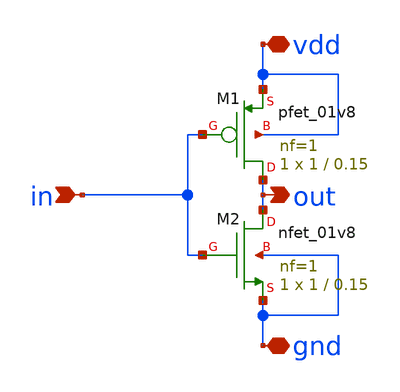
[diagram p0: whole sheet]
** sch_path: inverter.sch
**.subckt inverter in vdd gnd out
*.ipin in
*.iopin vdd
*.iopin gnd
*.opin out
XM1 out in vdd vdd sky130_fd_pr__pfet_01v8 L=0.15 W=1 nf=1 ad='int((1 + 1)/2) * 1 / 1 * 0.29' as='int((1 + 2)/2) * 1 / 1 * 0.29'
+ pd='2*int((1 + 1)/2) * (1 / 1 + 0.29)' ps='2*int((1 + 2)/2) * (1 / 1 + 0.29)' nrd='0.29 / 1 ' nrs='0.29 / 1 '
+ sa=0 sb=0 sd=0 mult=1 m=1
XM2 out in gnd gnd sky130_fd_pr__nfet_01v8 L=0.15 W=1 nf=1 ad='int((1 + 1)/2) * 1 / 1 * 0.29' as='int((1 + 2)/2) * 1 / 1 * 0.29'
+ pd='2*int((1 + 1)/2) * (1 / 1 + 0.29)' ps='2*int((1 + 2)/2) * (1 / 1 + 0.29)' nrd='0.29 / 1 ' nrs='0.29 / 1 '
+ sa=0 sb=0 sd=0 mult=1 m=1
**.ends
.end
